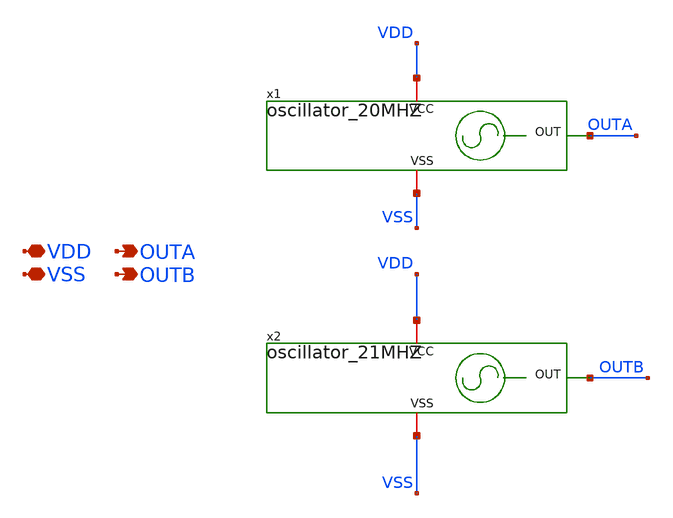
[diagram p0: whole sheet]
** sch_path: xschem/top.sch
**.subckt top VDD VSS OUTA OUTB
*.iopin VDD
*.iopin VSS
*.opin OUTA
*.opin OUTB
x1 VDD OUTA VSS oscillator_20MHZ
x2 VDD OUTB VSS oscillator_21MHZ
**.ends

* expanding   symbol:  oscillator_20MHZ.sym # of pins=3
** sym_path: xschem/oscillator_20MHZ.sym
** sch_path: xschem/oscillator_20MHZ.sch
.subckt oscillator_20MHZ VCC OUT VSS
*.iopin VCC
*.iopin VSS
*.opin OUT
x1[99] INI[98] OUT VCC VSS inverter
x1[98] INI[97] INI[98] VCC VSS inverter
x1[97] INI[96] INI[97] VCC VSS inverter
x1[96] INI[95] INI[96] VCC VSS inverter
x1[95] INI[94] INI[95] VCC VSS inverter
x1[94] INI[93] INI[94] VCC VSS inverter
x1[93] INI[92] INI[93] VCC VSS inverter
x1[92] INI[91] INI[92] VCC VSS inverter
x1[91] INI[90] INI[91] VCC VSS inverter
x1[90] INI[89] INI[90] VCC VSS inverter
x1[89] INI[88] INI[89] VCC VSS inverter
x1[88] INI[87] INI[88] VCC VSS inverter
x1[87] INI[86] INI[87] VCC VSS inverter
x1[86] INI[85] INI[86] VCC VSS inverter
x1[85] INI[84] INI[85] VCC VSS inverter
x1[84] INI[83] INI[84] VCC VSS inverter
x1[83] INI[82] INI[83] VCC VSS inverter
x1[82] INI[81] INI[82] VCC VSS inverter
x1[81] INI[80] INI[81] VCC VSS inverter
x1[80] INI[79] INI[80] VCC VSS inverter
x1[79] INI[78] INI[79] VCC VSS inverter
x1[78] INI[77] INI[78] VCC VSS inverter
x1[77] INI[76] INI[77] VCC VSS inverter
x1[76] INI[75] INI[76] VCC VSS inverter
x1[75] INI[74] INI[75] VCC VSS inverter
x1[74] INI[73] INI[74] VCC VSS inverter
x1[73] INI[72] INI[73] VCC VSS inverter
x1[72] INI[71] INI[72] VCC VSS inverter
x1[71] INI[70] INI[71] VCC VSS inverter
x1[70] INI[69] INI[70] VCC VSS inverter
x1[69] INI[68] INI[69] VCC VSS inverter
x1[68] INI[67] INI[68] VCC VSS inverter
x1[67] INI[66] INI[67] VCC VSS inverter
x1[66] INI[65] INI[66] VCC VSS inverter
x1[65] INI[64] INI[65] VCC VSS inverter
x1[64] INI[63] INI[64] VCC VSS inverter
x1[63] INI[62] INI[63] VCC VSS inverter
x1[62] INI[61] INI[62] VCC VSS inverter
x1[61] INI[60] INI[61] VCC VSS inverter
x1[60] INI[59] INI[60] VCC VSS inverter
x1[59] INI[58] INI[59] VCC VSS inverter
x1[58] INI[57] INI[58] VCC VSS inverter
x1[57] INI[56] INI[57] VCC VSS inverter
x1[56] INI[55] INI[56] VCC VSS inverter
x1[55] INI[54] INI[55] VCC VSS inverter
x1[54] INI[53] INI[54] VCC VSS inverter
x1[53] INI[52] INI[53] VCC VSS inverter
x1[52] INI[51] INI[52] VCC VSS inverter
x1[51] INI[50] INI[51] VCC VSS inverter
x1[50] INI[49] INI[50] VCC VSS inverter
x1[49] INI[48] INI[49] VCC VSS inverter
x1[48] INI[47] INI[48] VCC VSS inverter
x1[47] INI[46] INI[47] VCC VSS inverter
x1[46] INI[45] INI[46] VCC VSS inverter
x1[45] INI[44] INI[45] VCC VSS inverter
x1[44] INI[43] INI[44] VCC VSS inverter
x1[43] INI[42] INI[43] VCC VSS inverter
x1[42] INI[41] INI[42] VCC VSS inverter
x1[41] INI[40] INI[41] VCC VSS inverter
x1[40] INI[39] INI[40] VCC VSS inverter
x1[39] INI[38] INI[39] VCC VSS inverter
x1[38] INI[37] INI[38] VCC VSS inverter
x1[37] INI[36] INI[37] VCC VSS inverter
x1[36] INI[35] INI[36] VCC VSS inverter
x1[35] INI[34] INI[35] VCC VSS inverter
x1[34] INI[33] INI[34] VCC VSS inverter
x1[33] INI[32] INI[33] VCC VSS inverter
x1[32] INI[31] INI[32] VCC VSS inverter
x1[31] INI[30] INI[31] VCC VSS inverter
x1[30] INI[29] INI[30] VCC VSS inverter
x1[29] INI[28] INI[29] VCC VSS inverter
x1[28] INI[27] INI[28] VCC VSS inverter
x1[27] INI[26] INI[27] VCC VSS inverter
x1[26] INI[25] INI[26] VCC VSS inverter
x1[25] INI[24] INI[25] VCC VSS inverter
x1[24] INI[23] INI[24] VCC VSS inverter
x1[23] INI[22] INI[23] VCC VSS inverter
x1[22] INI[21] INI[22] VCC VSS inverter
x1[21] INI[20] INI[21] VCC VSS inverter
x1[20] INI[19] INI[20] VCC VSS inverter
x1[19] INI[18] INI[19] VCC VSS inverter
x1[18] INI[17] INI[18] VCC VSS inverter
x1[17] INI[16] INI[17] VCC VSS inverter
x1[16] INI[15] INI[16] VCC VSS inverter
x1[15] INI[14] INI[15] VCC VSS inverter
x1[14] INI[13] INI[14] VCC VSS inverter
x1[13] INI[12] INI[13] VCC VSS inverter
x1[12] INI[11] INI[12] VCC VSS inverter
x1[11] INI[10] INI[11] VCC VSS inverter
x1[10] INI[9] INI[10] VCC VSS inverter
x1[9] INI[8] INI[9] VCC VSS inverter
x1[8] INI[7] INI[8] VCC VSS inverter
x1[7] INI[6] INI[7] VCC VSS inverter
x1[6] INI[5] INI[6] VCC VSS inverter
x1[5] INI[4] INI[5] VCC VSS inverter
x1[4] INI[3] INI[4] VCC VSS inverter
x1[3] INI[2] INI[3] VCC VSS inverter
x1[2] INI[1] INI[2] VCC VSS inverter
x1[1] INI[0] INI[1] VCC VSS inverter
x1[0] OUT INI[0] VCC VSS inverter
.ends


* expanding   symbol:  oscillator_21MHZ.sym # of pins=3
** sym_path: xschem/oscillator_21MHZ.sym
** sch_path: xschem/oscillator_21MHZ.sch
.subckt oscillator_21MHZ VCC OUT VSS
*.iopin VCC
*.iopin VSS
*.opin OUT
x1[99] INI[98] OUT VCC VSS inverter
x1[98] INI[97] INI[98] VCC VSS inverter
x1[97] INI[96] INI[97] VCC VSS inverter
x1[96] INI[95] INI[96] VCC VSS inverter
x1[95] INI[94] INI[95] VCC VSS inverter
x1[94] INI[93] INI[94] VCC VSS inverter
x1[93] INI[92] INI[93] VCC VSS inverter
x1[92] INI[91] INI[92] VCC VSS inverter
x1[91] INI[90] INI[91] VCC VSS inverter
x1[90] INI[89] INI[90] VCC VSS inverter
x1[89] INI[88] INI[89] VCC VSS inverter
x1[88] INI[87] INI[88] VCC VSS inverter
x1[87] INI[86] INI[87] VCC VSS inverter
x1[86] INI[85] INI[86] VCC VSS inverter
x1[85] INI[84] INI[85] VCC VSS inverter
x1[84] INI[83] INI[84] VCC VSS inverter
x1[83] INI[82] INI[83] VCC VSS inverter
x1[82] INI[81] INI[82] VCC VSS inverter
x1[81] INI[80] INI[81] VCC VSS inverter
x1[80] INI[79] INI[80] VCC VSS inverter
x1[79] INI[78] INI[79] VCC VSS inverter
x1[78] INI[77] INI[78] VCC VSS inverter
x1[77] INI[76] INI[77] VCC VSS inverter
x1[76] INI[75] INI[76] VCC VSS inverter
x1[75] INI[74] INI[75] VCC VSS inverter
x1[74] INI[73] INI[74] VCC VSS inverter
x1[73] INI[72] INI[73] VCC VSS inverter
x1[72] INI[71] INI[72] VCC VSS inverter
x1[71] INI[70] INI[71] VCC VSS inverter
x1[70] INI[69] INI[70] VCC VSS inverter
x1[69] INI[68] INI[69] VCC VSS inverter
x1[68] INI[67] INI[68] VCC VSS inverter
x1[67] INI[66] INI[67] VCC VSS inverter
x1[66] INI[65] INI[66] VCC VSS inverter
x1[65] INI[64] INI[65] VCC VSS inverter
x1[64] INI[63] INI[64] VCC VSS inverter
x1[63] INI[62] INI[63] VCC VSS inverter
x1[62] INI[61] INI[62] VCC VSS inverter
x1[61] INI[60] INI[61] VCC VSS inverter
x1[60] INI[59] INI[60] VCC VSS inverter
x1[59] INI[58] INI[59] VCC VSS inverter
x1[58] INI[57] INI[58] VCC VSS inverter
x1[57] INI[56] INI[57] VCC VSS inverter
x1[56] INI[55] INI[56] VCC VSS inverter
x1[55] INI[54] INI[55] VCC VSS inverter
x1[54] INI[53] INI[54] VCC VSS inverter
x1[53] INI[52] INI[53] VCC VSS inverter
x1[52] INI[51] INI[52] VCC VSS inverter
x1[51] INI[50] INI[51] VCC VSS inverter
x1[50] INI[49] INI[50] VCC VSS inverter
x1[49] INI[48] INI[49] VCC VSS inverter
x1[48] INI[47] INI[48] VCC VSS inverter
x1[47] INI[46] INI[47] VCC VSS inverter
x1[46] INI[45] INI[46] VCC VSS inverter
x1[45] INI[44] INI[45] VCC VSS inverter
x1[44] INI[43] INI[44] VCC VSS inverter
x1[43] INI[42] INI[43] VCC VSS inverter
x1[42] INI[41] INI[42] VCC VSS inverter
x1[41] INI[40] INI[41] VCC VSS inverter
x1[40] INI[39] INI[40] VCC VSS inverter
x1[39] INI[38] INI[39] VCC VSS inverter
x1[38] INI[37] INI[38] VCC VSS inverter
x1[37] INI[36] INI[37] VCC VSS inverter
x1[36] INI[35] INI[36] VCC VSS inverter
x1[35] INI[34] INI[35] VCC VSS inverter
x1[34] INI[33] INI[34] VCC VSS inverter
x1[33] INI[32] INI[33] VCC VSS inverter
x1[32] INI[31] INI[32] VCC VSS inverter
x1[31] INI[30] INI[31] VCC VSS inverter
x1[30] INI[29] INI[30] VCC VSS inverter
x1[29] INI[28] INI[29] VCC VSS inverter
x1[28] INI[27] INI[28] VCC VSS inverter
x1[27] INI[26] INI[27] VCC VSS inverter
x1[26] INI[25] INI[26] VCC VSS inverter
x1[25] INI[24] INI[25] VCC VSS inverter
x1[24] INI[23] INI[24] VCC VSS inverter
x1[23] INI[22] INI[23] VCC VSS inverter
x1[22] INI[21] INI[22] VCC VSS inverter
x1[21] INI[20] INI[21] VCC VSS inverter
x1[20] INI[19] INI[20] VCC VSS inverter
x1[19] INI[18] INI[19] VCC VSS inverter
x1[18] INI[17] INI[18] VCC VSS inverter
x1[17] INI[16] INI[17] VCC VSS inverter
x1[16] INI[15] INI[16] VCC VSS inverter
x1[15] INI[14] INI[15] VCC VSS inverter
x1[14] INI[13] INI[14] VCC VSS inverter
x1[13] INI[12] INI[13] VCC VSS inverter
x1[12] INI[11] INI[12] VCC VSS inverter
x1[11] INI[10] INI[11] VCC VSS inverter
x1[10] INI[9] INI[10] VCC VSS inverter
x1[9] INI[8] INI[9] VCC VSS inverter
x1[8] INI[7] INI[8] VCC VSS inverter
x1[7] INI[6] INI[7] VCC VSS inverter
x1[6] INI[5] INI[6] VCC VSS inverter
x1[5] INI[4] INI[5] VCC VSS inverter
x1[4] INI[3] INI[4] VCC VSS inverter
x1[3] INI[2] INI[3] VCC VSS inverter
x1[2] INI[1] INI[2] VCC VSS inverter
x1[1] INI[0] INI[1] VCC VSS inverter
x1[0] OUT INI[0] VCC VSS inverter
.ends


* expanding   symbol:  inverter.sym # of pins=4
** sym_path: xschem/inverter.sym
** sch_path: xschem/inverter.sch
.subckt inverter OUT IN VCC VSS
*.iopin VCC
*.iopin VSS
*.ipin IN
*.opin OUT
XM1 OUT IN net1 VCC sky130_fd_pr__pfet_01v8 L=1 W=2 nf=1 ad='int((nf+1)/2) * W/nf * 0.29' as='int((nf+2)/2) * W/nf * 0.29'
+ pd='2*int((nf+1)/2) * (W/nf + 0.29)' ps='2*int((nf+2)/2) * (W/nf + 0.29)' nrd='0.29 / W' nrs='0.29 / W'
+ sa=0 sb=0 sd=0 mult=1 m=1
XM2 OUT IN net2 VSS sky130_fd_pr__nfet_01v8 L=1 W=1 nf=1 ad='int((nf+1)/2) * W/nf * 0.29' as='int((nf+2)/2) * W/nf * 0.29'
+ pd='2*int((nf+1)/2) * (W/nf + 0.29)' ps='2*int((nf+2)/2) * (W/nf + 0.29)' nrd='0.29 / W' nrs='0.29 / W'
+ sa=0 sb=0 sd=0 mult=1 m=1
XM3 net1 VSS VCC VCC sky130_fd_pr__pfet_01v8 L=1 W=2 nf=1 ad='int((nf+1)/2) * W/nf * 0.29' as='int((nf+2)/2) * W/nf * 0.29'
+ pd='2*int((nf+1)/2) * (W/nf + 0.29)' ps='2*int((nf+2)/2) * (W/nf + 0.29)' nrd='0.29 / W' nrs='0.29 / W'
+ sa=0 sb=0 sd=0 mult=1 m=1
XM4 net2 VCC VSS VSS sky130_fd_pr__nfet_01v8 L=1 W=1 nf=1 ad='int((nf+1)/2) * W/nf * 0.29' as='int((nf+2)/2) * W/nf * 0.29'
+ pd='2*int((nf+1)/2) * (W/nf + 0.29)' ps='2*int((nf+2)/2) * (W/nf + 0.29)' nrd='0.29 / W' nrs='0.29 / W'
+ sa=0 sb=0 sd=0 mult=1 m=1
.ends

.end
